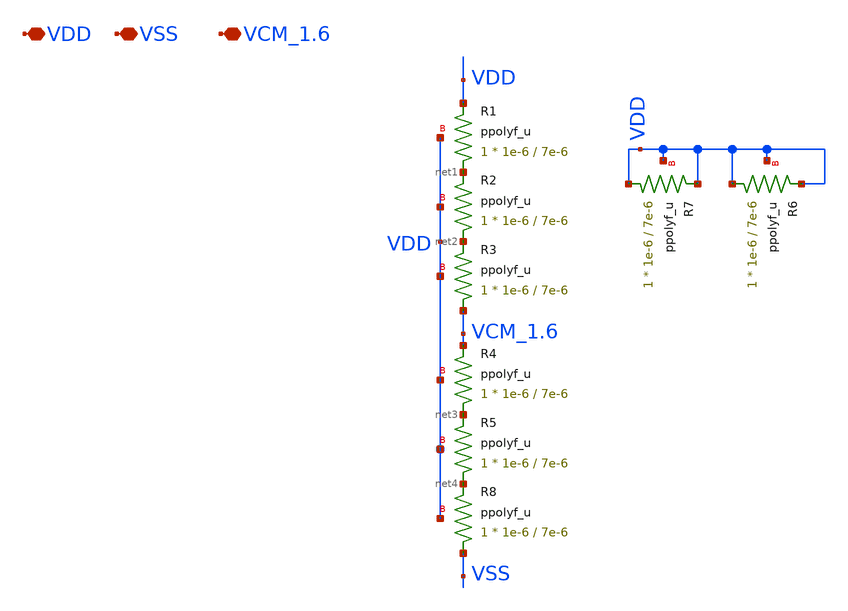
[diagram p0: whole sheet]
** sch_path: AWG_OUTPUT_AND_MUX_PAKISTAN_05/xschem/RES_VCM_1.6.sch
**.subckt RES_VCM_1.6 VDD VSS VCM_1.6
*.iopin VDD
*.iopin VSS
*.iopin VCM_1.6
XR1 net1 VDD VDD ppolyf_u r_width=1e-6 r_length=7e-6 m=1
XR2 net2 net1 VDD ppolyf_u r_width=1e-6 r_length=7e-6 m=1
XR3 VCM_1.6 net2 VDD ppolyf_u r_width=1e-6 r_length=7e-6 m=1
XR4 net3 VCM_1.6 VDD ppolyf_u r_width=1e-6 r_length=7e-6 m=1
XR5 net4 net3 VDD ppolyf_u r_width=1e-6 r_length=7e-6 m=1
XR6 VDD VDD VDD ppolyf_u r_width=1e-6 r_length=7e-6 m=1
XR7 VDD VDD VDD ppolyf_u r_width=1e-6 r_length=7e-6 m=1
XR8 VSS net4 VDD ppolyf_u r_width=1e-6 r_length=7e-6 m=1
**.ends
.end
